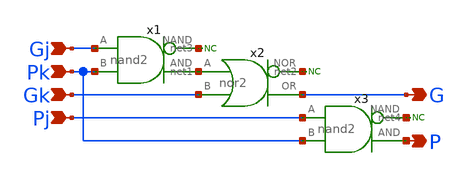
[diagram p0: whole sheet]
** sch_path: elements/ks_black.sch
**.subckt ks_black G Pk Gj Gk P Pj
*.opin G
*.ipin Pk
*.ipin Gj
*.ipin Gk
*.opin P
*.ipin Pj
x2 net1 G Gk net2 nor2
* noconn #net2
x1 net3 net1 Gj Pk nand2
* noconn #net3
x3 net4 P Pj Pk nand2
* noconn #net4
**.ends
.end
